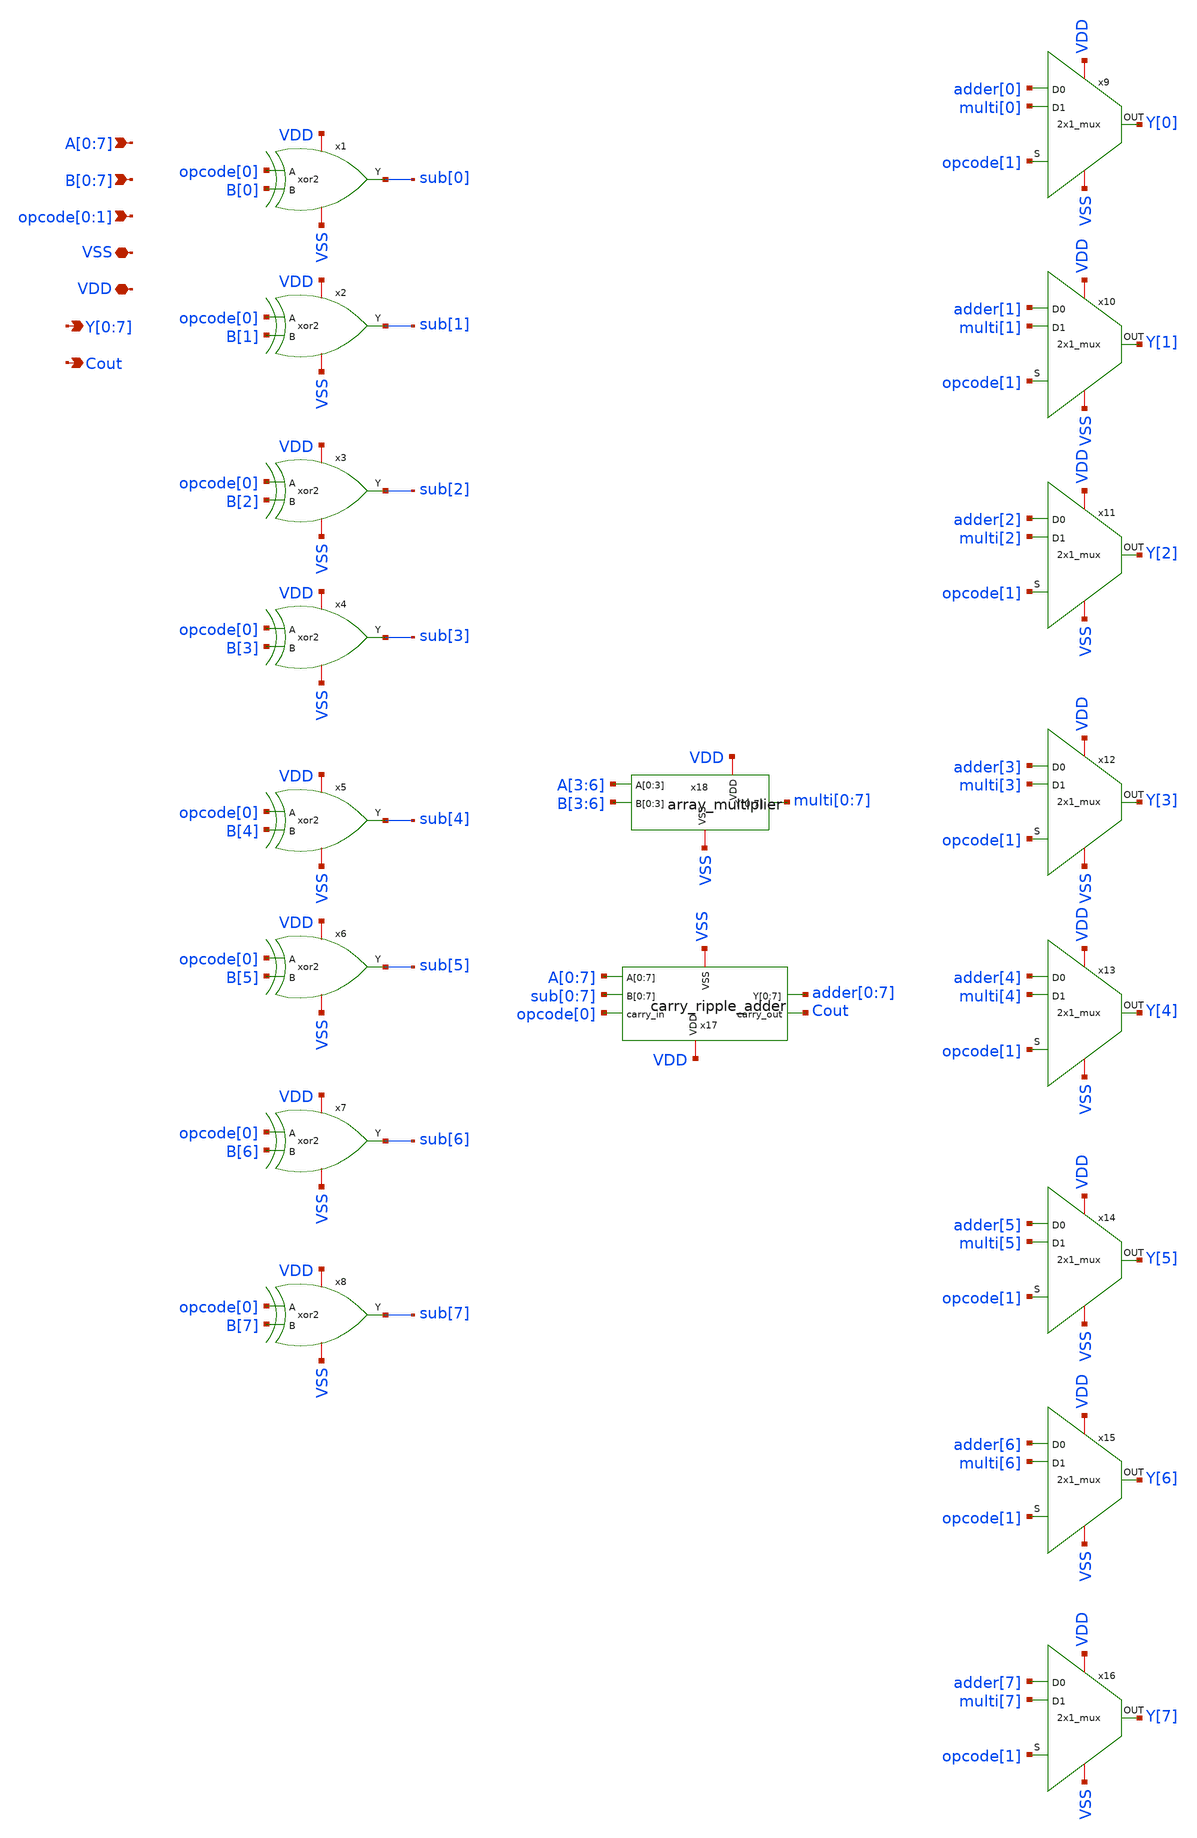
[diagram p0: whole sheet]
** sch_path: design/ARITMETIC_UNIT/xschem/arithmetic_unit.sch
**.subckt arithmetic_unit A[0],A[1],A[2],A[3],A[4],A[5],A[6],A[7]
*+ B[0],B[1],B[2],B[3],B[4],B[5],B[6],B[7] opcode[0],opcode[1] Y[0],Y[1],Y[2],Y[3],Y[4],Y[5],Y[6],Y[7] Cout VSS VDD
*.ipin A[0],A[1],A[2],A[3],A[4],A[5],A[6],A[7]
*.ipin B[0],B[1],B[2],B[3],B[4],B[5],B[6],B[7]
*.ipin opcode[0],opcode[1]
*.opin Y[0],Y[1],Y[2],Y[3],Y[4],Y[5],Y[6],Y[7]
*.opin Cout
*.iopin VSS
*.iopin VDD
x1 sub[0] opcode[0] VDD VSS B[0] xor2
x2 sub[1] opcode[0] VDD VSS B[1] xor2
x3 sub[2] opcode[0] VDD VSS B[2] xor2
x4 sub[3] opcode[0] VDD VSS B[3] xor2
x5 sub[4] opcode[0] VDD VSS B[4] xor2
x6 sub[5] opcode[0] VDD VSS B[5] xor2
x7 sub[6] opcode[0] VDD VSS B[6] xor2
x8 sub[7] opcode[0] VDD VSS B[7] xor2
x9 VSS VDD opcode[1] adder[0] multi[0] Y[0] 2x1_mux
x10 VSS VDD opcode[1] adder[1] multi[1] Y[1] 2x1_mux
x11 VSS VDD opcode[1] adder[2] multi[2] Y[2] 2x1_mux
x12 VSS VDD opcode[1] adder[3] multi[3] Y[3] 2x1_mux
x13 VSS VDD opcode[1] adder[4] multi[4] Y[4] 2x1_mux
x14 VSS VDD opcode[1] adder[5] multi[5] Y[5] 2x1_mux
x15 VSS VDD opcode[1] adder[6] multi[6] Y[6] 2x1_mux
x16 VSS VDD opcode[1] adder[7] multi[7] Y[7] 2x1_mux
x18 A[3] A[4] A[5] A[6] B[3] B[4] B[5] B[6] VDD VSS multi[0] multi[1] multi[2] multi[3] multi[4]
+ multi[5] multi[6] multi[7] array_multiplier
x17 A[0] A[1] A[2] A[3] A[4] A[5] A[6] A[7] sub[0] sub[1] sub[2] sub[3] sub[4] sub[5] sub[6] sub[7]
+ opcode[0] VDD VSS adder[0] adder[1] adder[2] adder[3] adder[4] adder[5] adder[6] adder[7] Cout
+ carry_ripple_adder
**.ends
.end
